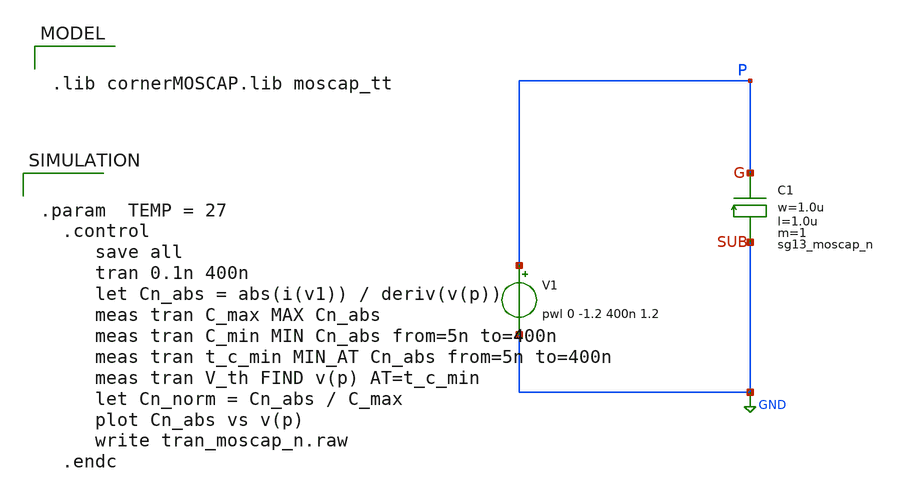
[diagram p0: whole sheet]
** sch_path: ihp-sg13g2/libs.tech/xschem/sg13g2_tests/tran_moscap_n.sch
**.subckt tran_moscap_n
V1 P GND pwl 0 -1.2 400n 1.2
XC1 P GND sg13_moscap_n w=1.0u l=1.0u m=1 mm_ok=1
**** begin user architecture code


.lib cornerMOSCAP.lib moscap_tt




.param  TEMP = 27
  .control
     save all
     tran 0.1n 400n
     let Cn_abs = abs(i(v1)) / deriv(v(p))
     meas tran C_max MAX Cn_abs
     meas tran C_min MIN Cn_abs from=5n to=400n
     meas tran t_c_min MIN_AT Cn_abs from=5n to=400n
     meas tran V_th FIND v(p) AT=t_c_min
     let Cn_norm = Cn_abs / C_max
     plot Cn_abs vs v(p)
     write tran_moscap_n.raw
  .endc


**** end user architecture code
**.ends
.GLOBAL GND
.end
